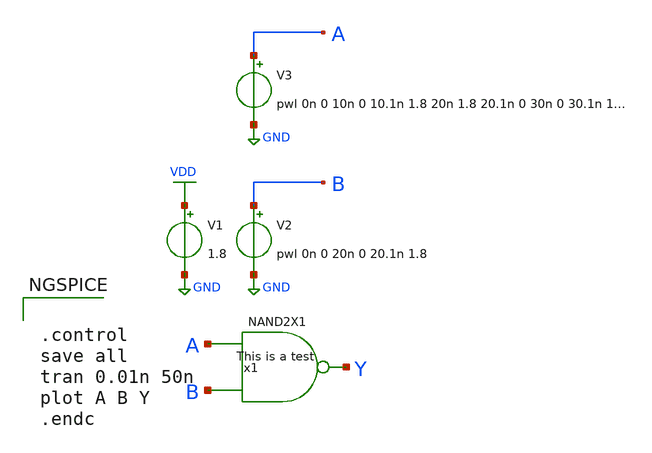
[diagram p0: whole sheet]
** sch_path: archives/lib/xschem/test_NAND2X1.sch
**.subckt test_NAND2X1
V2 B GND pwl 0n 0 20n 0 20.1n 1.8
V1 VDD GND 1.8
V3 A GND pwl 0n 0 10n 0 10.1n 1.8 20n 1.8 20.1n 0 30n 0 30.1n 1.8 40n 1.8 40.1n 0
x1 Y A B VDD GND NAND2X1
**** begin user architecture code

.lib $::SKYWATER_MODELS/sky130.lib.spice tt


**** end user architecture code
**.ends
.GLOBAL VDD
.GLOBAL GND
**** begin user architecture code


.control
save all
tran 0.01n 50n
plot A B Y
.endc


**** end user architecture code
.end
